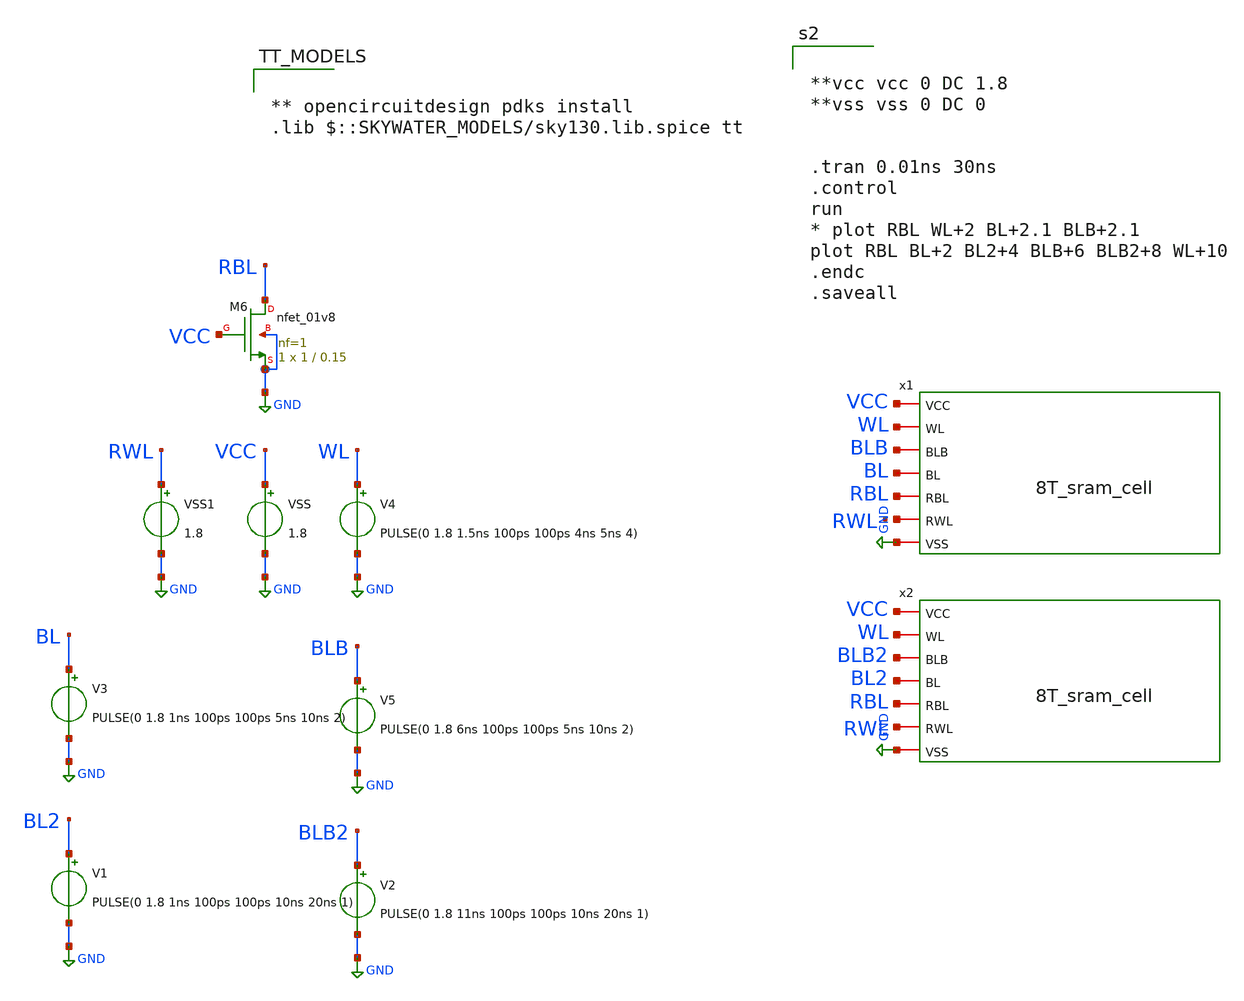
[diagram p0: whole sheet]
** sch_path: 8Tsram_test - Copy.sch
**.subckt 8Tsram_test - Copy
V3 BL GND PULSE(0 1.8 1ns 100ps 100ps 5ns 10ns 2)
V4 WL GND PULSE(0 1.8 1.5ns 100ps 100ps 4ns 5ns 4)
V5 BLB GND PULSE(0 1.8 6ns 100ps 100ps 5ns 10ns 2)
VSS VCC GND 1.8
XM6 RBL VCC GND GND sky130_fd_pr__nfet_01v8 L=0.15 W=1 nf=1 ad='int((1 + 1)/2) * 1 / 1 * 0.29' as='int((1 + 2)/2) * 1 / 1 * 0.29'
+ pd='2*int((1 + 1)/2) * (1 / 1 + 0.29)' ps='2*int((1 + 2)/2) * (1 / 1 + 0.29)' nrd='0.29 / 1 ' nrs='0.29 / 1 '
+ sa=0 sb=0 sd=0 mult=1 m=1
x1 VCC WL BLB BL RBL net1 GND 8T_sram_cell
VSS1 RWL GND 1.8
x2 VCC WL BLB2 BL2 RBL RWL GND 8T_sram_cell
V1 BL2 GND PULSE(0 1.8 1ns 100ps 100ps 10ns 20ns 1)
V2 BLB2 GND PULSE(0 1.8 11ns 100ps 100ps 10ns 20ns 1)
**** begin user architecture code


**vcc vcc 0 DC 1.8
**vss vss 0 DC 0


.tran 0.01ns 30ns
.control
run
* plot RBL WL+2 BL+2.1 BLB+2.1
plot RBL BL+2 BL2+4 BLB+6 BLB2+8 WL+10
.endc
.saveall




** opencircuitdesign pdks install
.lib $::SKYWATER_MODELS/sky130.lib.spice tt

**** end user architecture code
**.ends

* expanding   symbol:  8T_sram_cell.sym # of pins=7
** sym_path: 8T_sram_cell.sym
** sch_path: 8T_sram_cell.sch
.subckt 8T_sram_cell VCC WL BLB BL RBL RWL VSS
*.iopin VCC
*.iopin BLB
*.iopin WL
*.iopin BL
*.iopin VSS
*.iopin RBL
*.iopin RWL
XM1 q_bar q VSS VSS sky130_fd_pr__nfet_01v8 L=0.15 W=1 nf=1 ad='int((1 + 1)/2) * 1 / 1 * 0.29' as='int((1 + 2)/2) * 1 / 1 * 0.29'
+ pd='2*int((1 + 1)/2) * (1 / 1 + 0.29)' ps='2*int((1 + 2)/2) * (1 / 1 + 0.29)' nrd='0.29 / 1 ' nrs='0.29 / 1 '
+ sa=0 sb=0 sd=0 mult=1 m=1
XM2 q q_bar VSS VSS sky130_fd_pr__nfet_01v8 L=0.15 W=1 nf=1 ad='int((1 + 1)/2) * 1 / 1 * 0.29' as='int((1 + 2)/2) * 1 / 1 * 0.29'
+ pd='2*int((1 + 1)/2) * (1 / 1 + 0.29)' ps='2*int((1 + 2)/2) * (1 / 1 + 0.29)' nrd='0.29 / 1 ' nrs='0.29 / 1 '
+ sa=0 sb=0 sd=0 mult=1 m=1
XM3 q_bar q VCC VCC sky130_fd_pr__pfet_01v8 L=0.15 W=4 nf=1 ad='int((1 + 1)/2) * 4 / 1 * 0.29' as='int((1 + 2)/2) * 4 / 1 * 0.29'
+ pd='2*int((1 + 1)/2) * (4 / 1 + 0.29)' ps='2*int((1 + 2)/2) * (4 / 1 + 0.29)' nrd='0.29 / 4 ' nrs='0.29 / 4 '
+ sa=0 sb=0 sd=0 mult=1 m=1
XM4 q q_bar VCC VCC sky130_fd_pr__pfet_01v8 L=0.15 W=4 nf=1 ad='int((1 + 1)/2) * 4 / 1 * 0.29' as='int((1 + 2)/2) * 4 / 1 * 0.29'
+ pd='2*int((1 + 1)/2) * (4 / 1 + 0.29)' ps='2*int((1 + 2)/2) * (4 / 1 + 0.29)' nrd='0.29 / 4 ' nrs='0.29 / 4 '
+ sa=0 sb=0 sd=0 mult=1 m=1
XM5 BLB WL q_bar VSS sky130_fd_pr__nfet_01v8 L=0.15 W=1 nf=1 ad='int((1 + 1)/2) * 1 / 1 * 0.29' as='int((1 + 2)/2) * 1 / 1 * 0.29'
+ pd='2*int((1 + 1)/2) * (1 / 1 + 0.29)' ps='2*int((1 + 2)/2) * (1 / 1 + 0.29)' nrd='0.29 / 1 ' nrs='0.29 / 1 '
+ sa=0 sb=0 sd=0 mult=1 m=1
XM8 q WL BL VSS sky130_fd_pr__nfet_01v8 L=0.15 W=1 nf=1 ad='int((1 + 1)/2) * 1 / 1 * 0.29' as='int((1 + 2)/2) * 1 / 1 * 0.29'
+ pd='2*int((1 + 1)/2) * (1 / 1 + 0.29)' ps='2*int((1 + 2)/2) * (1 / 1 + 0.29)' nrd='0.29 / 1 ' nrs='0.29 / 1 '
+ sa=0 sb=0 sd=0 mult=1 m=1
XM6 net1 q_bar VSS VSS sky130_fd_pr__nfet_01v8 L=0.15 W=1 nf=1 ad='int((1 + 1)/2) * 1 / 1 * 0.29' as='int((1 + 2)/2) * 1 / 1 * 0.29'
+ pd='2*int((1 + 1)/2) * (1 / 1 + 0.29)' ps='2*int((1 + 2)/2) * (1 / 1 + 0.29)' nrd='0.29 / 1 ' nrs='0.29 / 1 '
+ sa=0 sb=0 sd=0 mult=1 m=1
XM7 RBL RWL net1 VSS sky130_fd_pr__nfet_01v8 L=0.15 W=1 nf=1 ad='int((1 + 1)/2) * 1 / 1 * 0.29' as='int((1 + 2)/2) * 1 / 1 * 0.29'
+ pd='2*int((1 + 1)/2) * (1 / 1 + 0.29)' ps='2*int((1 + 2)/2) * (1 / 1 + 0.29)' nrd='0.29 / 1 ' nrs='0.29 / 1 '
+ sa=0 sb=0 sd=0 mult=1 m=1
.ends

.GLOBAL GND
.end
